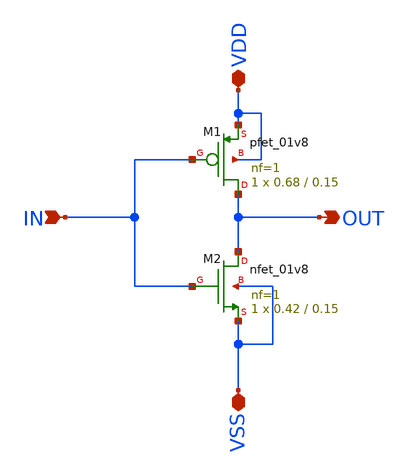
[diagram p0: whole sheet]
** sch_path: inv.sch
**.subckt inv IN OUT VDD VSS
*.ipin IN
*.opin OUT
*.iopin VDD
*.iopin VSS
XM1 OUT IN VDD VDD sky130_fd_pr__pfet_01v8 L=0.15 W=0.68 nf=1 ad='int((1 + 1)/2) * 0.68 / 1 * 0.29' as='int((1 + 2)/2) * 0.68 / 1 * 0.29'
+ pd='2*int((1 + 1)/2) * (0.68 / 1 + 0.29)' ps='2*int((1 + 2)/2) * (0.68 / 1 + 0.29)' nrd='0.29 / 0.68 '
+ nrs='0.29 / 0.68 ' sa=0 sb=0 sd=0 mult=1 m=1
XM2 OUT IN VSS VSS sky130_fd_pr__nfet_01v8 L=0.15 W=0.42 nf=1 ad='int((1 + 1)/2) * 0.42 / 1 * 0.29' as='int((1 + 2)/2) * 0.42 / 1 * 0.29'
+ pd='2*int((1 + 1)/2) * (0.42 / 1 + 0.29)' ps='2*int((1 + 2)/2) * (0.42 / 1 + 0.29)' nrd='0.29 / 0.42 '
+ nrs='0.29 / 0.42 ' sa=0 sb=0 sd=0 mult=1 m=1
**.ends
.end
